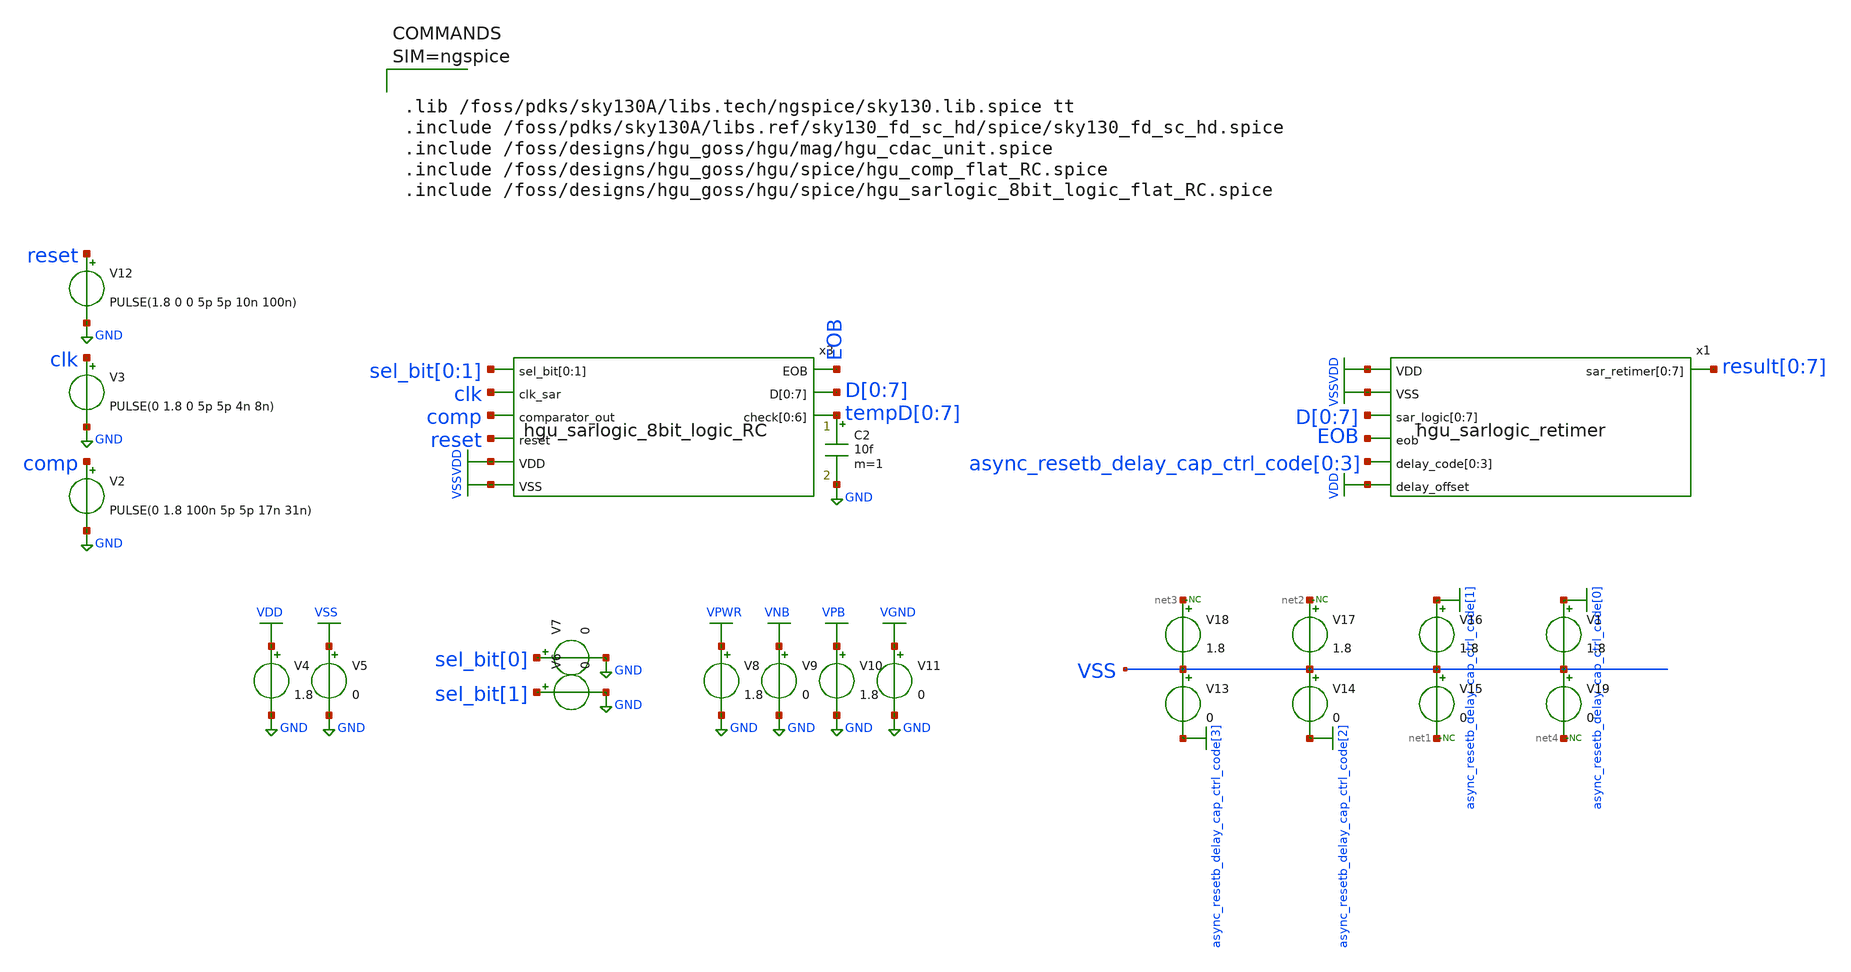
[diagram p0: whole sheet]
** sch_path: hgu/tb/tb_hgu_sarlogic_8bit_logic.sch
**.subckt tb_hgu_sarlogic_8bit_logic
V4 VDD GND 1.8
V5 VSS GND 0
V8 VPWR GND 1.8
V9 VNB GND 0
V10 VPB GND 1.8
V11 VGND GND 0
V6 sel_bit[1] GND 0
V7 sel_bit[0] GND 0
V2 comp GND PULSE(0 1.8 100n 5p 5p 17n 31n)
V3 clk GND PULSE(0 1.8 0 5p 5p 4n 8n)
V12 reset GND PULSE(1.8 0 0 5p 5p 10n 100n)
x3 sel_bit[0] sel_bit[1] EOB clk D[0] D[1] D[2] D[3] D[4] D[5] D[6] D[7] comp tempD[0] tempD[1]
+ tempD[2] tempD[3] tempD[4] tempD[5] tempD[6] reset VDD VSS hgu_sarlogic_8bit_logic_RC
C2 tempD[0] GND 10f m=1
x1 VDD VSS D[0] D[1] D[2] D[3] D[4] D[5] D[6] D[7] EOB async_resetb_delay_cap_ctrl_code[0]
+ async_resetb_delay_cap_ctrl_code[1] async_resetb_delay_cap_ctrl_code[2] async_resetb_delay_cap_ctrl_code[3] VDD result[0] result[1]
+ result[2] result[3] result[4] result[5] result[6] result[7] hgu_sarlogic_retimer
V1 async_resetb_delay_cap_ctrl_code[0] VSS 1.8
V13 VSS async_resetb_delay_cap_ctrl_code[3] 0
V14 VSS async_resetb_delay_cap_ctrl_code[2] 0
V15 VSS net1 0
V16 async_resetb_delay_cap_ctrl_code[1] VSS 1.8
V17 net2 VSS 1.8
V18 net3 VSS 1.8
V19 VSS net4 0
* noconn #net3
* noconn #net2
* noconn #net1
* noconn #net4
**** begin user architecture code





*.tran 10ps 310ns
.tran 40ps 300ns

.control
	option temp = 25
	let vdd_act = 1.8

	alter V1 vdd_act

	run
	plot V("tempD[0]") V("tempD[1]")+2 V("tempD[2]")+4 V("tempD[3]")+6 V("tempD[4]")+8 V("tempD[5]")+10
+ V("tempD[6]")+12 V("tempD[7]")+14 V(clk)-4 V(EOB)-2
	plot V(comp) V(clk)+2 V(EOB)+4 V("D[0]")+6 V("D[1]")+8 V("D[2]")+10 V("D[3]")+12  V("D[4]")+14
+ V("D[5]")+16 V("D[6]")+18 V("D[7]")+20 V(reset)-2

 .endc
.save all






.lib /foss/pdks/sky130A/libs.tech/ngspice/sky130.lib.spice tt
.include /foss/pdks/sky130A/libs.ref/sky130_fd_sc_hd/spice/sky130_fd_sc_hd.spice
.include /foss/designs/hgu_goss/hgu/mag/hgu_cdac_unit.spice
.include /foss/designs/hgu_goss/hgu/spice/hgu_comp_flat_RC.spice
.include /foss/designs/hgu_goss/hgu/spice/hgu_sarlogic_8bit_logic_flat_RC.spice



**** end user architecture code
**.ends
.GLOBAL VDD
.GLOBAL GND
.GLOBAL VSS
.GLOBAL VGND
.GLOBAL VNB
.GLOBAL VPB
.GLOBAL VPWR
.GLOBAL async_resetb_delay_cap_ctrl_code[3]
.GLOBAL async_resetb_delay_cap_ctrl_code[2]
.GLOBAL async_resetb_delay_cap_ctrl_code[1]
.GLOBAL async_resetb_delay_cap_ctrl_code[0]
.end
